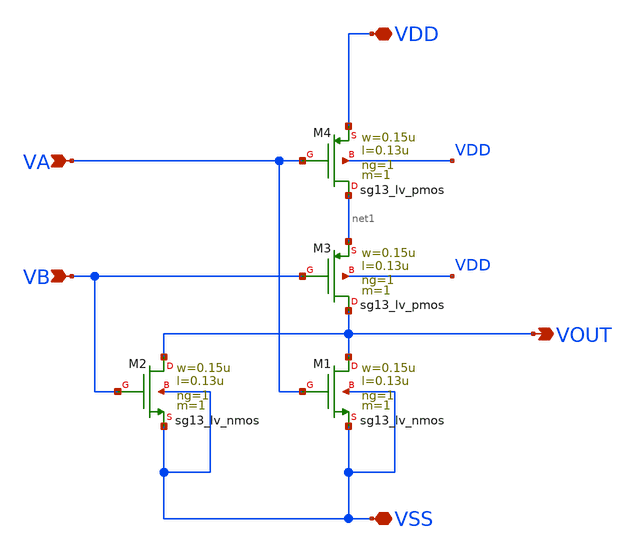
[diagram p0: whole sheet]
** sch_path: ADC8711-main/schematic/xschem/NOR.sch
**.subckt NOR VDD VSS VA VB VOUT
*.iopin VDD
*.iopin VSS
*.ipin VA
*.ipin VB
*.opin VOUT
XM1 VOUT VA VSS VSS sg13_lv_nmos w=0.15u l=0.13u ng=1 m=1 mm_ok=1
XM2 VOUT VB VSS VSS sg13_lv_nmos w=0.15u l=0.13u ng=1 m=1 mm_ok=1
XM3 VOUT VB net1 VDD sg13_lv_pmos w=0.15u l=0.13u ng=1 m=1 mm_ok=1
XM4 net1 VA VDD VDD sg13_lv_pmos w=0.15u l=0.13u ng=1 m=1 mm_ok=1
**.ends
.end
